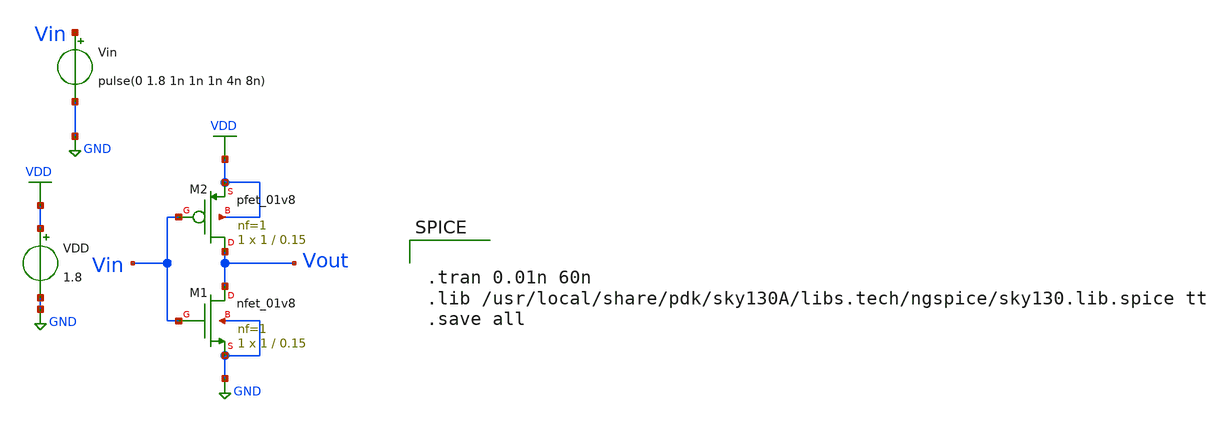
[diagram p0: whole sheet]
** sch_path: week1/designs/xschem/pre-layout/inverter_trans.sch
**.subckt inverter_trans
XM1 Vout Vin GND GND sky130_fd_pr__nfet_01v8 L=0.15 W=1 nf=1 ad='int((nf+1)/2) * W/nf * 0.29' as='int((nf+2)/2) * W/nf * 0.29'
+ pd='2*int((nf+1)/2) * (W/nf + 0.29)' ps='2*int((nf+2)/2) * (W/nf + 0.29)' nrd='0.29 / W' nrs='0.29 / W'
+ sa=0 sb=0 sd=0 mult=1 m=1
XM2 Vout Vin VDD VDD sky130_fd_pr__pfet_01v8 L=0.15 W=1 nf=1 ad='int((nf+1)/2) * W/nf * 0.29' as='int((nf+2)/2) * W/nf * 0.29'
+ pd='2*int((nf+1)/2) * (W/nf + 0.29)' ps='2*int((nf+2)/2) * (W/nf + 0.29)' nrd='0.29 / W' nrs='0.29 / W'
+ sa=0 sb=0 sd=0 mult=1 m=1
VDD VDD GND 1.8
Vin Vin GND pulse(0 1.8 1n 1n 1n 4n 8n)
**** begin user architecture code


.tran 0.01n 60n
.lib /usr/local/share/pdk/sky130A/libs.tech/ngspice/sky130.lib.spice tt
.save all

**** end user architecture code
**.ends
.GLOBAL GND
.GLOBAL VDD
.end
